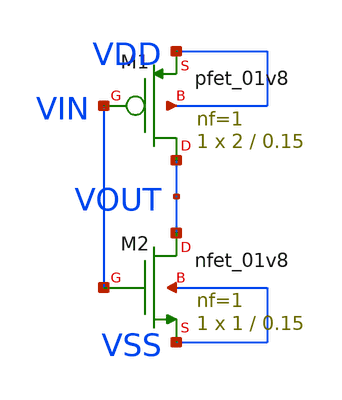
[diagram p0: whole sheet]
** sch_path: My_Inverter/inverter_sky130.sch
**.subckt inverter_sky130
XM1 VOUT VIN VDD VDD sky130_fd_pr__pfet_01v8 L=0.15 W=2 nf=1 ad='int((nf+1)/2) * W/nf * 0.29' as='int((nf+2)/2) * W/nf * 0.29'
+ pd='2*int((nf+1)/2) * (W/nf + 0.29)' ps='2*int((nf+2)/2) * (W/nf + 0.29)' nrd='0.29 / W' nrs='0.29 / W'
+ sa=0 sb=0 sd=0 mult=1 m=1
XM2 VOUT VIN VSS VSS sky130_fd_pr__nfet_01v8 L=0.15 W=1 nf=1 ad='int((1 + 1)/2) * 1 / 1 * 0.29' as='int((1 + 2)/2) * 1 / 1 * 0.29'
+ pd='2*int((1 + 1)/2) * (1 / 1 + 0.29)' ps='2*int((1 + 2)/2) * (1 / 1 + 0.29)' nrd='0.29 / 1 ' nrs='0.29 / 1 '
+ sa=0 sb=0 sd=0 mult=1 m=1
**.ends
.end
